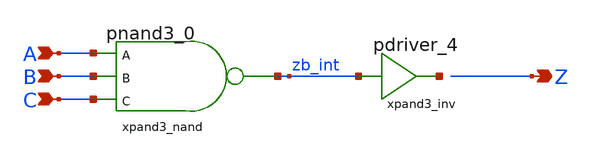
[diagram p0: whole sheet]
** sch_path: sram_2_64_scn4m/pand3.sch
**.subckt pand3 A B C Z
*.ipin A
*.ipin B
*.ipin C
*.opin Z
xpand3_nand A B C zb_int vdd gnd pnand3_0
xpand3_inv zb_int net1 pdriver_4
**.ends
.end
